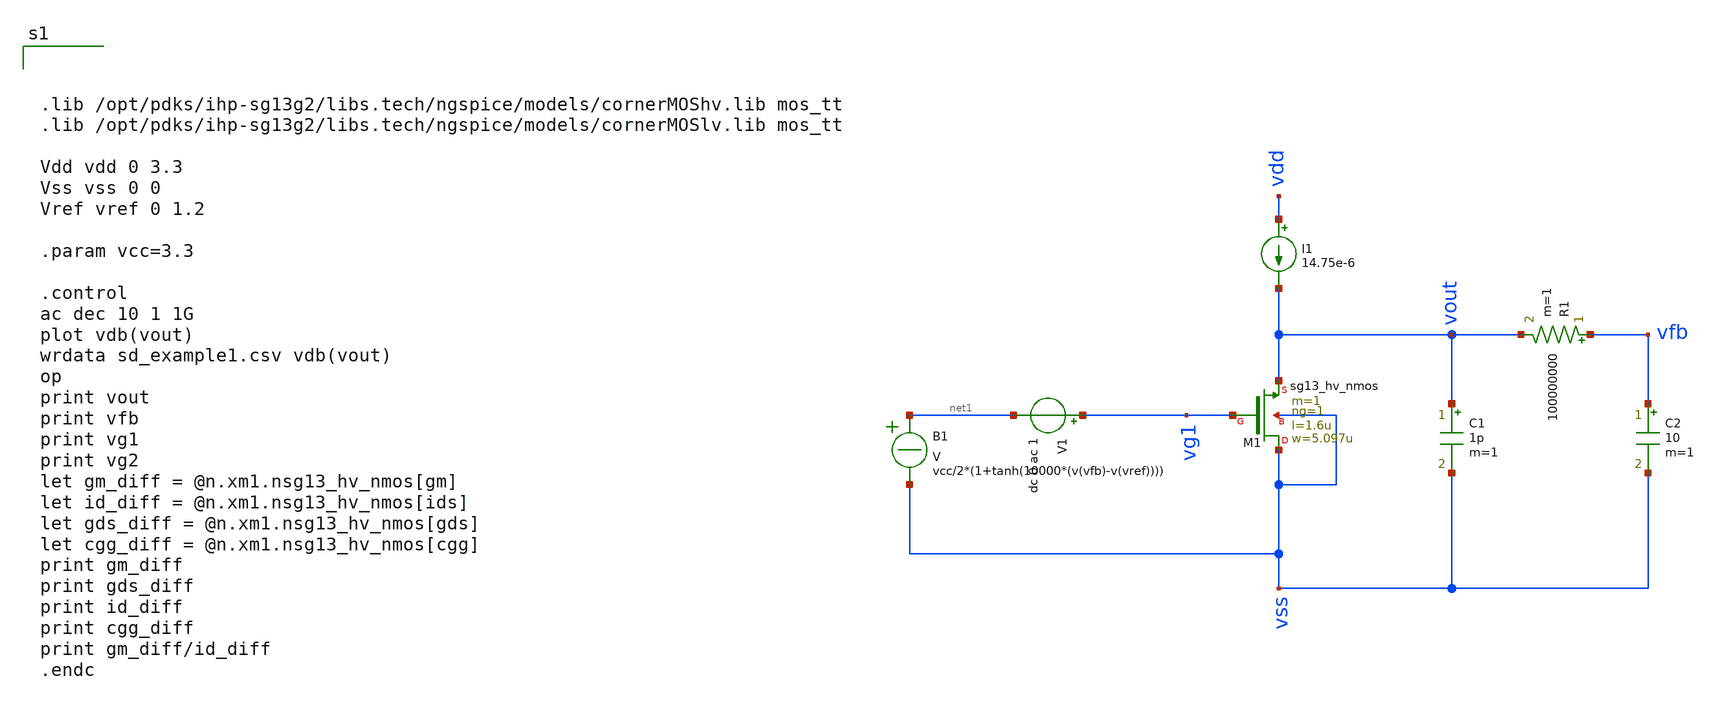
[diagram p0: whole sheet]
** sch_path: test/sstadex/xschem/sd_example.sch
**.subckt sd_example
XM1 vss vg1 vout vss sg13_hv_nmos w=5.097u l=1.6u ng=1 m=1 mm_ok=1
C1 vout vss 1p m=1
I1 vdd vout 14.75e-6
B1 net1 vss V = vcc/2*(1+tanh(10000*(v(vfb)-v(vref))))
V1 vg1 net1 dc 0 ac 1
R1 vfb vout 100000000 m=1
C2 vfb vss 10 m=1
**** begin user architecture code



.lib /opt/pdks/ihp-sg13g2/libs.tech/ngspice/models/cornerMOShv.lib mos_tt
.lib /opt/pdks/ihp-sg13g2/libs.tech/ngspice/models/cornerMOSlv.lib mos_tt

Vdd vdd 0 3.3
Vss vss 0 0
Vref vref 0 1.2

.param vcc=3.3

.control
ac dec 10 1 1G
plot vdb(vout)
wrdata sd_example1.csv vdb(vout)
op
print vout
print vfb
print vg1
print vg2
let gm_diff = @n.xm1.nsg13_hv_nmos[gm]
let id_diff = @n.xm1.nsg13_hv_nmos[ids]
let gds_diff = @n.xm1.nsg13_hv_nmos[gds]
let cgg_diff = @n.xm1.nsg13_hv_nmos[cgg]
print gm_diff
print gds_diff
print id_diff
print cgg_diff
print gm_diff/id_diff
.endc



**** end user architecture code
**.ends
.end
